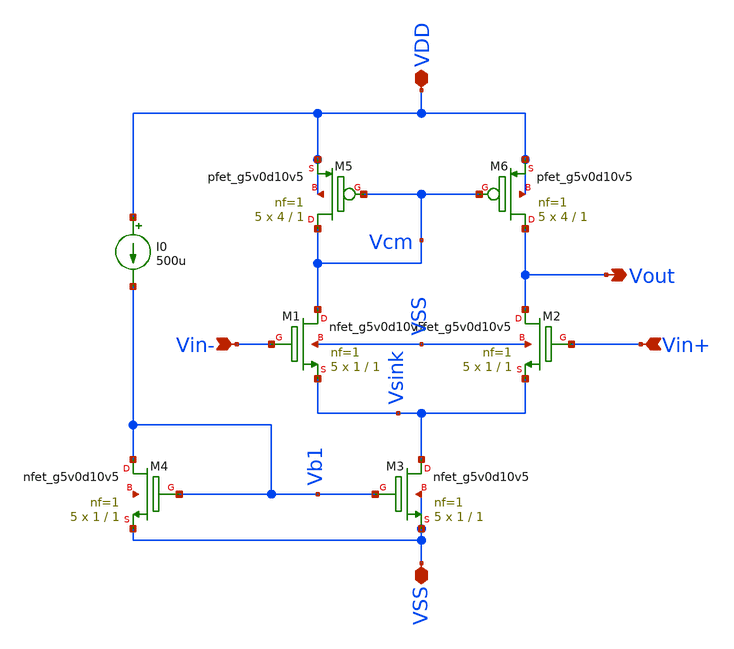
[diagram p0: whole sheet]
** sch_path: xschem/Amplifiers/5T.sch
**.subckt 5T VDD VSS Vin- Vin+ Vout
*.iopin VDD
*.iopin VSS
*.ipin Vin-
*.ipin Vin+
*.opin Vout
I0 VDD Vb1 500u
XM1 Vcm Vin- Vsink VSS sky130_fd_pr__nfet_g5v0d10v5 L=1 W=1 nf=1 ad='int((nf+1)/2) * W/nf * 0.29' as='int((nf+2)/2) * W/nf * 0.29'
+ pd='2*int((nf+1)/2) * (W/nf + 0.29)' ps='2*int((nf+2)/2) * (W/nf + 0.29)' nrd='0.29 / W' nrs='0.29 / W'
+ sa=0 sb=0 sd=0 mult=5 m=5
XM2 Vout Vin+ Vsink VSS sky130_fd_pr__nfet_g5v0d10v5 L=1 W=1 nf=1 ad='int((nf+1)/2) * W/nf * 0.29' as='int((nf+2)/2) * W/nf * 0.29'
+ pd='2*int((nf+1)/2) * (W/nf + 0.29)' ps='2*int((nf+2)/2) * (W/nf + 0.29)' nrd='0.29 / W' nrs='0.29 / W'
+ sa=0 sb=0 sd=0 mult=5 m=5
XM3 Vsink Vb1 VSS VSS sky130_fd_pr__nfet_g5v0d10v5 L=1 W=1 nf=1 ad='int((nf+1)/2) * W/nf * 0.29' as='int((nf+2)/2) * W/nf * 0.29'
+ pd='2*int((nf+1)/2) * (W/nf + 0.29)' ps='2*int((nf+2)/2) * (W/nf + 0.29)' nrd='0.29 / W' nrs='0.29 / W'
+ sa=0 sb=0 sd=0 mult=5 m=5
XM4 Vb1 Vb1 VSS net1 sky130_fd_pr__nfet_g5v0d10v5 L=1 W=1 nf=1 ad='int((nf+1)/2) * W/nf * 0.29' as='int((nf+2)/2) * W/nf * 0.29'
+ pd='2*int((nf+1)/2) * (W/nf + 0.29)' ps='2*int((nf+2)/2) * (W/nf + 0.29)' nrd='0.29 / W' nrs='0.29 / W'
+ sa=0 sb=0 sd=0 mult=5 m=5
XM5 Vcm Vcm VDD VDD sky130_fd_pr__pfet_g5v0d10v5 L=1 W=4 nf=1 ad='int((nf+1)/2) * W/nf * 0.29' as='int((nf+2)/2) * W/nf * 0.29'
+ pd='2*int((nf+1)/2) * (W/nf + 0.29)' ps='2*int((nf+2)/2) * (W/nf + 0.29)' nrd='0.29 / W' nrs='0.29 / W'
+ sa=0 sb=0 sd=0 mult=5 m=5
XM6 Vout Vcm VDD VDD sky130_fd_pr__pfet_g5v0d10v5 L=1 W=4 nf=1 ad='int((nf+1)/2) * W/nf * 0.29' as='int((nf+2)/2) * W/nf * 0.29'
+ pd='2*int((nf+1)/2) * (W/nf + 0.29)' ps='2*int((nf+2)/2) * (W/nf + 0.29)' nrd='0.29 / W' nrs='0.29 / W'
+ sa=0 sb=0 sd=0 mult=5 m=5
**.ends
.end
